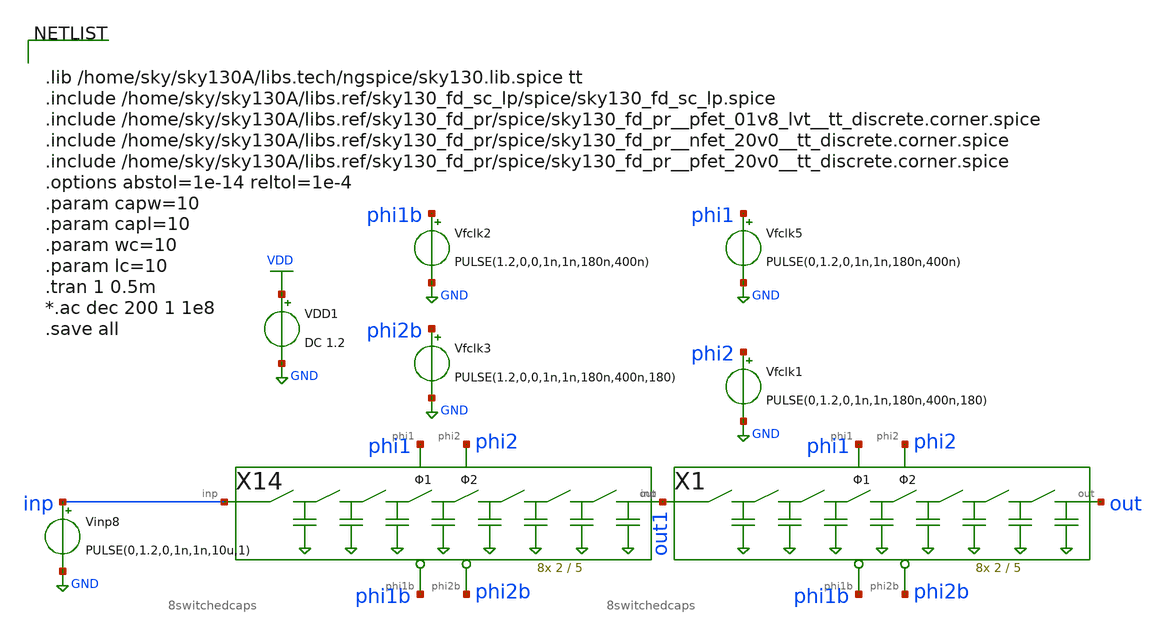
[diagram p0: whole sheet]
** sch_path: xschem/tryandtest/archive/gauss.sch
**.subckt gauss
VDD1 VDD GND DC 1.2
Vfclk5 phi1 GND PULSE(0,1.2,0,1n,1n,180n,400n)
Vfclk1 phi2 GND PULSE(0,1.2,0,1n,1n,180n,400n,180)
Vfclk2 phi1b GND PULSE(1.2,0,0,1n,1n,180n,400n)
Vfclk3 phi2b GND PULSE(1.2,0,0,1n,1n,180n,400n,180)
Vinp8 inp GND PULSE(0,1.2,0,1n,1n,10u,1)
X14 inp out1 phi2 phi1 phi1b phi2b 8switchedcaps Wcap=2 Lcap=5
X1 out1 out phi2 phi1 phi1b phi2b 8switchedcaps Wcap=2 Lcap=5
**** begin user architecture code


.lib /home/sky/sky130A/libs.tech/ngspice/sky130.lib.spice tt
.include /home/sky/sky130A/libs.ref/sky130_fd_sc_lp/spice/sky130_fd_sc_lp.spice
.include /home/sky/sky130A/libs.ref/sky130_fd_pr/spice/sky130_fd_pr__pfet_01v8_lvt__tt_discrete.corner.spice
.include /home/sky/sky130A/libs.ref/sky130_fd_pr/spice/sky130_fd_pr__nfet_20v0__tt_discrete.corner.spice
.include /home/sky/sky130A/libs.ref/sky130_fd_pr/spice/sky130_fd_pr__pfet_20v0__tt_discrete.corner.spice
.options abstol=1e-14 reltol=1e-4
.param capw=10
.param capl=10
.param wc=10
.param lc=10
.tran 1 0.5m
*.ac dec 200 1 1e8
.save all


**** end user architecture code
**.ends
.GLOBAL GND
.GLOBAL VDD
.end
